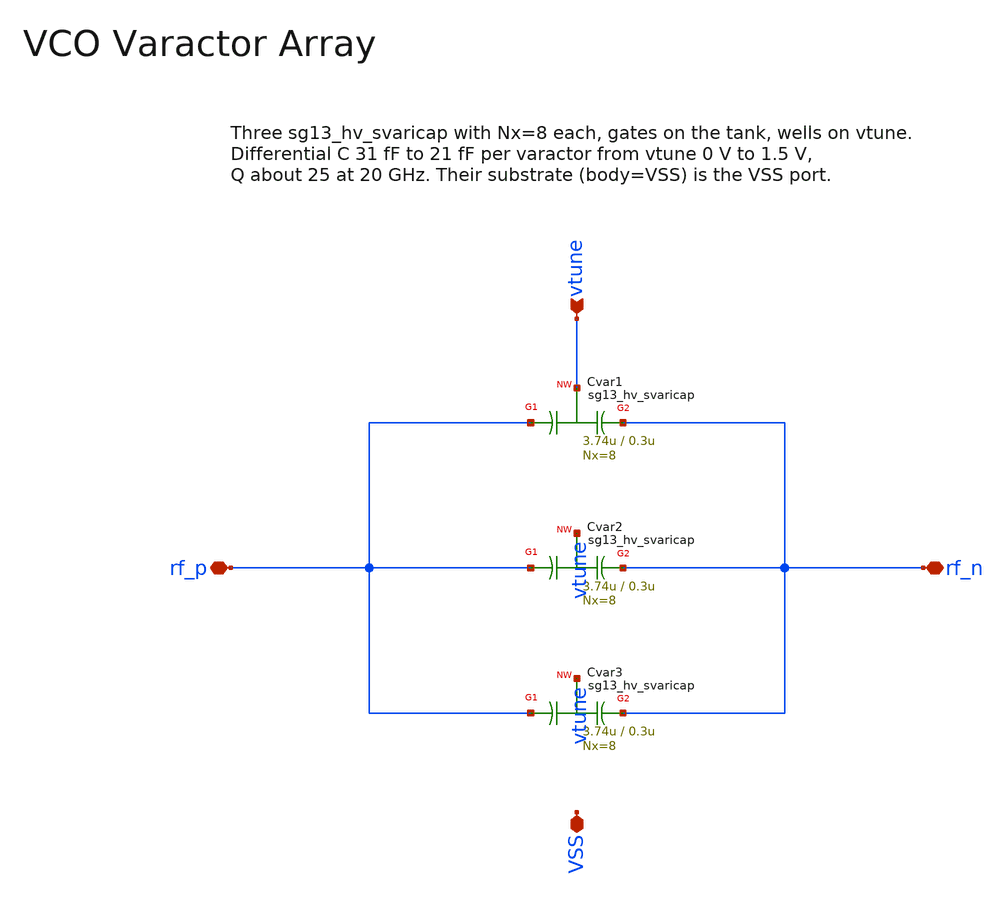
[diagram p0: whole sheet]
** sch_path: macros/vco/schematic/xschem/vco_var.sch
**.subckt vco_var vtune rf_p rf_n VSS
*.ipin vtune
*.iopin rf_p
*.iopin rf_n
*.iopin VSS
XCvar1 rf_p vtune rf_n VSS sg13_hv_svaricap w=3.74u l=0.3u Nx=8 mm_ok=1
XCvar2 rf_p vtune rf_n VSS sg13_hv_svaricap w=3.74u l=0.3u Nx=8 mm_ok=1
XCvar3 rf_p vtune rf_n VSS sg13_hv_svaricap w=3.74u l=0.3u Nx=8 mm_ok=1
**.ends
.end
